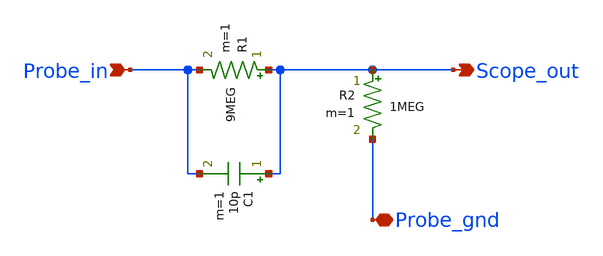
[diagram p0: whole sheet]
** sch_path: designs/simulation_parasitics/schematics/10x_attenuation_probe.sch
**.subckt 10x_attenuation_probe Probe_gnd Probe_in Scope_out
*.iopin Probe_gnd
*.ipin Probe_in
*.opin Scope_out
R1 Scope_out Probe_in 9MEG m=1
C1 Scope_out Probe_in 10p m=1
R2 Scope_out Probe_gnd 1MEG m=1
**.ends
.end
